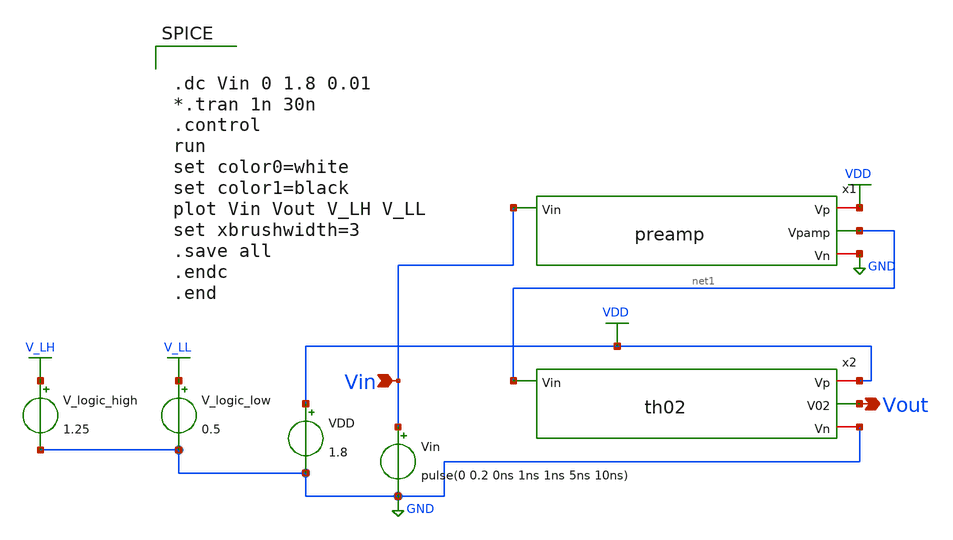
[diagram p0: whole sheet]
** sch_path: xschem/Vth_sch/Pre_layout/th02.sch
**.subckt th02 Vin Vout
*.ipin Vin
*.opin Vout
VDD VDD GND 1.8
Vin Vin GND pulse(0 0.2 0ns 1ns 1ns 5ns 10ns)
V_logic_high V_LH GND 1.25
V_logic_low V_LL GND 0.5
x1 VDD Vin net1 GND preamp
x2 VDD net1 Vout GND th02
**** begin user architecture code


.lib /usr/local/share/pdk/sky130A/libs.tech/ngspice/sky130.lib.spice tt

.save all





.dc Vin 0 1.8 0.01
*.tran 1n 30n
.control
run
set color0=white
set color1=black
plot Vin Vout V_LH V_LL
set xbrushwidth=3
.save all
.endc
.end


**** end user architecture code
**.ends

* expanding   symbol:  /home/exotic/Desktop/ASIC_ADC/xschem/Vth_sch/Symbol/preamp.sym # of pins=4
** sym_path: xschem/Vth_sch/Symbol/preamp.sym
** sch_path: xschem/Vth_sch/Symbol/preamp.sch
.subckt preamp Vp Vin Vpamp Vn
*.ipin Vin
*.opin Vpamp
*.iopin Vp
*.iopin Vn
XM1 Vp Vin Vpamp Vn sky130_fd_pr__nfet_01v8 L=3.5 W=1 nf=1 ad='int((nf+1)/2) * W/nf * 0.29' as='int((nf+2)/2) * W/nf * 0.29'
+ pd='2*int((nf+1)/2) * (W/nf + 0.29)' ps='2*int((nf+2)/2) * (W/nf + 0.29)' nrd='0.29 / W' nrs='0.29 / W'
+ sa=0 sb=0 sd=0 mult=1 m=1
XM0 Vn Vin Vpamp Vp sky130_fd_pr__pfet_01v8 L=0.150 W=0.63 nf=1 ad='int((nf+1)/2) * W/nf * 0.29' as='int((nf+2)/2) * W/nf * 0.29'
+ pd='2*int((nf+1)/2) * (W/nf + 0.29)' ps='2*int((nf+2)/2) * (W/nf + 0.29)' nrd='0.29 / W' nrs='0.29 / W'
+ sa=0 sb=0 sd=0 mult=1 m=1
.ends


* expanding   symbol:  /home/exotic/Desktop/ASIC_ADC/xschem/Vth_sch/Symbol/th02.sym # of pins=4
** sym_path: xschem/Vth_sch/Symbol/th02.sym
** sch_path: xschem/Vth_sch/Symbol/th02.sch
.subckt th02 Vp Vin V02 Vn
*.ipin Vin
*.opin V02
*.iopin Vp
*.iopin Vn
XM3 V02 net1 Vp Vp sky130_fd_pr__pfet_01v8 L=0.15 W=1.5 nf=1 ad='int((nf+1)/2) * W/nf * 0.29' as='int((nf+2)/2) * W/nf * 0.29'
+ pd='2*int((nf+1)/2) * (W/nf + 0.29)' ps='2*int((nf+2)/2) * (W/nf + 0.29)' nrd='0.29 / W' nrs='0.29 / W'
+ sa=0 sb=0 sd=0 mult=1 m=1
XM4 V02 net1 Vn Vn sky130_fd_pr__nfet_01v8 L=1.50 W=0.36 nf=1 ad='int((nf+1)/2) * W/nf * 0.29' as='int((nf+2)/2) * W/nf * 0.29'
+ pd='2*int((nf+1)/2) * (W/nf + 0.29)' ps='2*int((nf+2)/2) * (W/nf + 0.29)' nrd='0.29 / W' nrs='0.29 / W'
+ sa=0 sb=0 sd=0 mult=1 m=1
XM1 net1 Vin net2 Vp sky130_fd_pr__pfet_01v8 L=1.53 W=0.42 nf=1 ad='int((nf+1)/2) * W/nf * 0.29' as='int((nf+2)/2) * W/nf * 0.29'
+ pd='2*int((nf+1)/2) * (W/nf + 0.29)' ps='2*int((nf+2)/2) * (W/nf + 0.29)' nrd='0.29 / W' nrs='0.29 / W'
+ sa=0 sb=0 sd=0 mult=1 m=1
XM0 net1 Vin Vn Vn sky130_fd_pr__nfet_01v8 L=0.15 W=1.5 nf=2 ad='int((nf+1)/2) * W/nf * 0.29' as='int((nf+2)/2) * W/nf * 0.29'
+ pd='2*int((nf+1)/2) * (W/nf + 0.29)' ps='2*int((nf+2)/2) * (W/nf + 0.29)' nrd='0.29 / W' nrs='0.29 / W'
+ sa=0 sb=0 sd=0 mult=1 m=1
XM2 Vp Vp net2 Vn sky130_fd_pr__nfet_01v8 L=1.54 W=0.36 nf=1 ad='int((nf+1)/2) * W/nf * 0.29' as='int((nf+2)/2) * W/nf * 0.29'
+ pd='2*int((nf+1)/2) * (W/nf + 0.29)' ps='2*int((nf+2)/2) * (W/nf + 0.29)' nrd='0.29 / W' nrs='0.29 / W'
+ sa=0 sb=0 sd=0 mult=1 m=1
.ends

.GLOBAL VDD
.GLOBAL GND
.GLOBAL V_LH
.GLOBAL V_LL
.end
